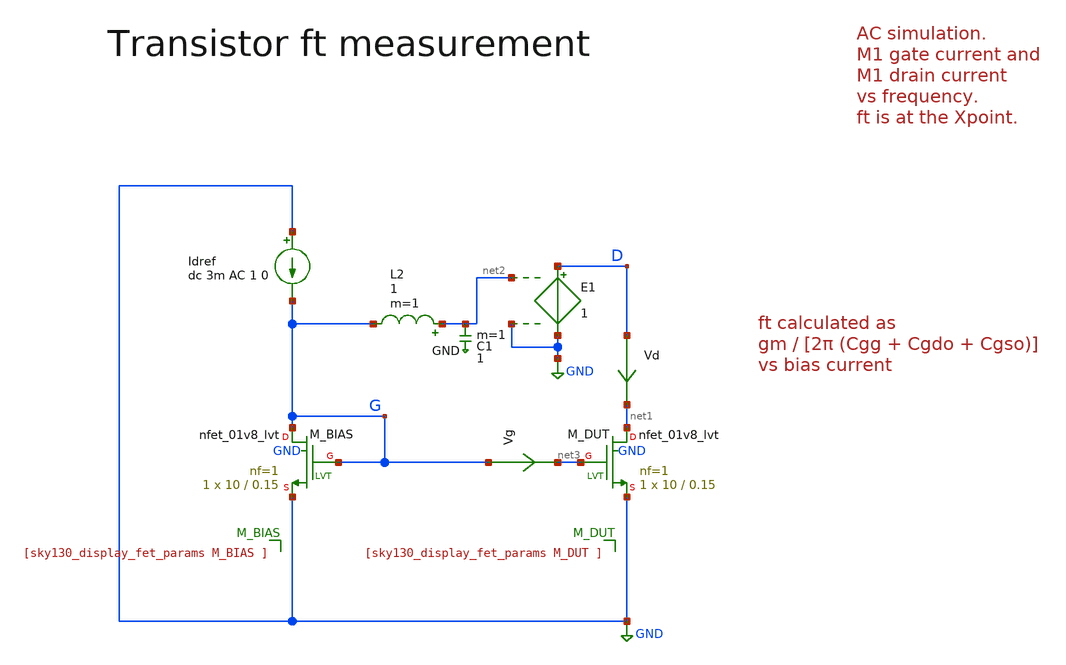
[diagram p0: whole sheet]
** sch_path: sky130A/xschem_libs/sky130_tests_ase/tb_ft_test/schematic/tb_ft_test.sch
* Copyright 2021 Stefan Frederik Schippers
* Licensed under the Apache License, Version 2.0 (the "License");
* you may not use this file except in compliance with the License.
* You may obtain a copy of the License at
* https://www.apache.org/licenses/LICENSE-2.0
* Unless required by applicable law or agreed to in writing, software
* distributed under the License is distributed on an "AS IS" BASIS,
* WITHOUT WARRANTIES OR CONDITIONS OF ANY KIND, either express or implied.
* See the License for the specific language governing permissions and
* limitations under the License.
**.subckt tb_ft_test
XM_DUT net1 net3 GND GND sky130_fd_pr__nfet_01v8_lvt L=0.15 W=10 nf=1 ad='int((1 + 1)/2) * 10 / 1 * 0.29'
+ as='int((1 + 2)/2) * 10 / 1 * 0.29' pd='2*int((1 + 1)/2) * (10 / 1 + 0.29)' ps='2*int((1 + 2)/2) * (10 / 1 + 0.29)'
+ nrd='0.29 / 10 ' nrs='0.29 / 10 ' sa=0 sb=0 sd=0 mult=1 m=1
Idref GND G dc 3m AC 1 0
Vd D net1 0
.save i(vd)
Vg G net3 0
.save i(vg)
XM_BIAS G G GND GND sky130_fd_pr__nfet_01v8_lvt L=0.15 W=10 nf=1 ad='int((1 + 1)/2) * 10 / 1 * 0.29'
+ as='int((1 + 2)/2) * 10 / 1 * 0.29' pd='2*int((1 + 1)/2) * (10 / 1 + 0.29)' ps='2*int((1 + 2)/2) * (10 / 1 + 0.29)'
+ nrd='0.29 / 10 ' nrs='0.29 / 10 ' sa=0 sb=0 sd=0 mult=1 m=1
L2 net2 G 1 m=1
C1 net2 GND 1 m=1
E1 D GND net2 GND 1
**.ends
.GLOBAL GND
.end
